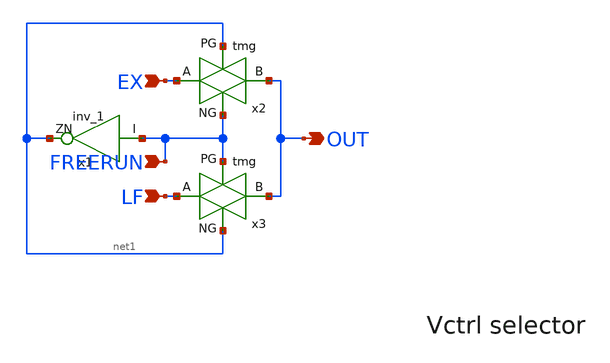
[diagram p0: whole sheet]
** sch_path: PLL/xschem/ctrlsel.sch
**.subckt ctrlsel OUT EX LF FREERUN
*.opin OUT
*.ipin EX
*.ipin LF
*.ipin FREERUN
x1 FREERUN net1 VDD VDD 0 0 gf180mcu_fd_sc_mcu7t5v0__inv_1
x2 net1 OUT EX FREERUN tmg
x3 FREERUN OUT LF net1 tmg
**.ends

* expanding   symbol:  tmg.sym # of pins=4
** sym_path: PLL/xschem/tmg.sym
** sch_path: PLL/xschem/tmg.sch
.subckt tmg PG B A NG
*.opin B
*.ipin A
*.ipin PG
*.ipin NG
XM3 B PG A VDD pfet_06v0 L=0.50u W=2u nf=1 ad='int((nf+1)/2) * W/nf * 0.18u' as='int((nf+2)/2) * W/nf * 0.18u'
+ pd='2*int((nf+1)/2) * (W/nf + 0.18u)' ps='2*int((nf+2)/2) * (W/nf + 0.18u)' nrd='0.18u / W' nrs='0.18u / W'
+ sa=0 sb=0 sd=0 m=1
XM4 A NG B GND nfet_06v0 L=0.60u W=0.9u nf=1 ad='int((nf+1)/2) * W/nf * 0.18u' as='int((nf+2)/2) * W/nf * 0.18u'
+ pd='2*int((nf+1)/2) * (W/nf + 0.18u)' ps='2*int((nf+2)/2) * (W/nf + 0.18u)' nrd='0.18u / W' nrs='0.18u / W'
+ sa=0 sb=0 sd=0 m=1
.ends

.GLOBAL GND
.GLOBAL VDD
.end
